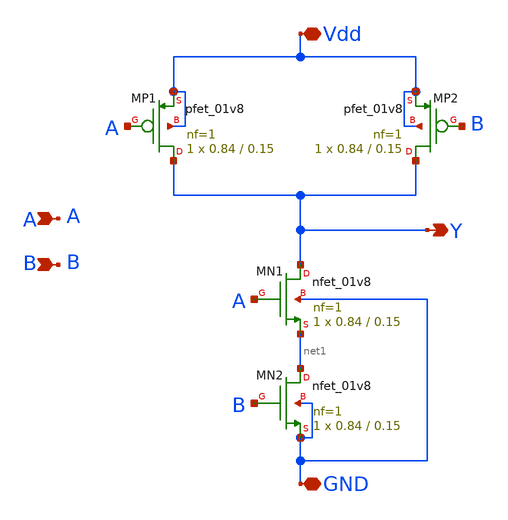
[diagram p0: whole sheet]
** sch_path: xschem_project/nand2/nand2_lvsclean.sch
**.subckt nand2_lvsclean A B Y Vdd GND
*.ipin A
*.ipin B
*.opin Y
*.iopin Vdd
*.iopin GND
XMP1 Y A Vdd Vdd sky130_fd_pr__pfet_01v8 L=0.15 W=0.84 nf=1 ad='int((1 + 1)/2) * 0.84 / 1 * 0.29' as='int((1 + 2)/2) * 0.84 / 1 * 0.29'
+ pd='2*int((1 + 1)/2) * (0.84 / 1 + 0.29)' ps='2*int((1 + 2)/2) * (0.84 / 1 + 0.29)' nrd='0.29 / 0.84 '
+ nrs='0.29 / 0.84 ' sa=0 sb=0 sd=0 mult=1 m=1
XMP2 Y B Vdd Vdd sky130_fd_pr__pfet_01v8 L=0.15 W=0.84 nf=1 ad='int((1 + 1)/2) * 0.84 / 1 * 0.29' as='int((1 + 2)/2) * 0.84 / 1 * 0.29'
+ pd='2*int((1 + 1)/2) * (0.84 / 1 + 0.29)' ps='2*int((1 + 2)/2) * (0.84 / 1 + 0.29)' nrd='0.29 / 0.84 '
+ nrs='0.29 / 0.84 ' sa=0 sb=0 sd=0 mult=1 m=1
XMN1 Y A net1 GND sky130_fd_pr__nfet_01v8 L=0.15 W=0.84 nf=1 ad='int((1 + 1)/2) * 0.84 / 1 * 0.29' as='int((1 + 2)/2) * 0.84 / 1 * 0.29'
+ pd='2*int((1 + 1)/2) * (0.84 / 1 + 0.29)' ps='2*int((1 + 2)/2) * (0.84 / 1 + 0.29)' nrd='0.29 / 0.84 '
+ nrs='0.29 / 0.84 ' sa=0 sb=0 sd=0 mult=1 m=1
XMN2 net1 B GND GND sky130_fd_pr__nfet_01v8 L=0.15 W=0.84 nf=1 ad='int((1 + 1)/2) * 0.84 / 1 * 0.29'
+ as='int((1 + 2)/2) * 0.84 / 1 * 0.29' pd='2*int((1 + 1)/2) * (0.84 / 1 + 0.29)' ps='2*int((1 + 2)/2) * (0.84 / 1 + 0.29)'
+ nrd='0.29 / 0.84 ' nrs='0.29 / 0.84 ' sa=0 sb=0 sd=0 mult=1 m=1
**.ends
.end
